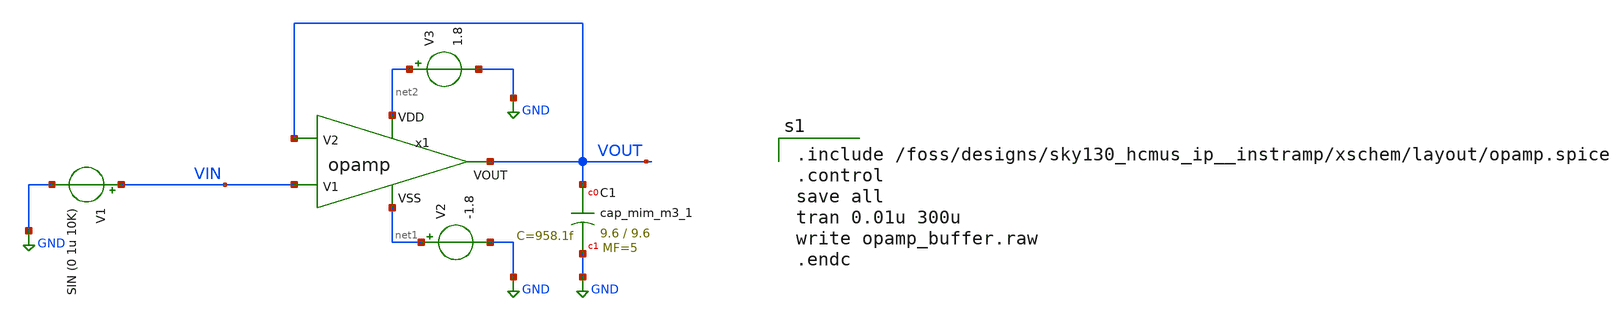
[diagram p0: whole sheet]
** sch_path: xschem/opamp_buffer.sch
**.subckt opamp_buffer
V3 net2 GND 1.8
V2 net1 GND -1.8
V1 VIN GND SIN (0 1u 10K)
x1 net2 net1 VIN VOUT VOUT opamp
XC1 VOUT GND sky130_fd_pr__cap_mim_m3_1 W=9.6 L=9.6 MF=5 m=5
**** begin user architecture code

** opencircuitdesign pdks install
.lib $::SKYWATER_MODELS/sky130.lib.spice tt



.include /foss/designs/sky130_hcmus_ip__instramp/xschem/layout/opamp.spice
.control
save all
tran 0.01u 300u
write opamp_buffer.raw
.endc


**** end user architecture code
**.ends

* expanding   symbol:  /foss/designs/sky130_hcmus_ip__instramp/xschem/opamp.sym # of pins=5
** sym_path: xschem/opamp.sym
** sch_path: xschem/opamp.sch
.subckt opamp VDD VSS V1 V2 VOUT
*.ipin VSS
*.ipin VDD
*.ipin V2
*.ipin V1
*.opin VOUT
XM2 net5 V2 net1 VSS sky130_fd_pr__nfet_01v8 L=1 W=8.5 nf=1 ad='int((nf+1)/2) * W/nf * 0.29' as='int((nf+2)/2) * W/nf * 0.29'
+ pd='2*int((nf+1)/2) * (W/nf + 0.29)' ps='2*int((nf+2)/2) * (W/nf + 0.29)' nrd='0.29 / W' nrs='0.29 / W'
+ sa=0 sb=0 sd=0 mult=1 m=1
XM1 net6 net5 VDD VDD sky130_fd_pr__pfet_01v8 L=1 W=41 nf=1 ad='int((nf+1)/2) * W/nf * 0.29' as='int((nf+2)/2) * W/nf * 0.29'
+ pd='2*int((nf+1)/2) * (W/nf + 0.29)' ps='2*int((nf+2)/2) * (W/nf + 0.29)' nrd='0.29 / W' nrs='0.29 / W'
+ sa=0 sb=0 sd=0 mult=1 m=1
XM4 net6 V1 net1 VSS sky130_fd_pr__nfet_01v8 L=1 W=8.5 nf=1 ad='int((nf+1)/2) * W/nf * 0.29' as='int((nf+2)/2) * W/nf * 0.29'
+ pd='2*int((nf+1)/2) * (W/nf + 0.29)' ps='2*int((nf+2)/2) * (W/nf + 0.29)' nrd='0.29 / W' nrs='0.29 / W'
+ sa=0 sb=0 sd=0 mult=1 m=1
XM5 net1 net4 VSS VSS sky130_fd_pr__nfet_01v8 L=1 W=20 nf=1 ad='int((nf+1)/2) * W/nf * 0.29' as='int((nf+2)/2) * W/nf * 0.29'
+ pd='2*int((nf+1)/2) * (W/nf + 0.29)' ps='2*int((nf+2)/2) * (W/nf + 0.29)' nrd='0.29 / W' nrs='0.29 / W'
+ sa=0 sb=0 sd=0 mult=1 m=1
XM6 VOUT net4 VSS VSS sky130_fd_pr__nfet_01v8 L=1 W=19 nf=1 ad='int((nf+1)/2) * W/nf * 0.29' as='int((nf+2)/2) * W/nf * 0.29'
+ pd='2*int((nf+1)/2) * (W/nf + 0.29)' ps='2*int((nf+2)/2) * (W/nf + 0.29)' nrd='0.29 / W' nrs='0.29 / W'
+ sa=0 sb=0 sd=0 mult=1 m=1
XM7 net4 net4 VSS VSS sky130_fd_pr__nfet_01v8 L=1 W=20 nf=1 ad='int((nf+1)/2) * W/nf * 0.29' as='int((nf+2)/2) * W/nf * 0.29'
+ pd='2*int((nf+1)/2) * (W/nf + 0.29)' ps='2*int((nf+2)/2) * (W/nf + 0.29)' nrd='0.29 / W' nrs='0.29 / W'
+ sa=0 sb=0 sd=0 mult=1 m=1
XM3 net5 net5 VDD VDD sky130_fd_pr__pfet_01v8 L=1 W=41 nf=1 ad='int((nf+1)/2) * W/nf * 0.29' as='int((nf+2)/2) * W/nf * 0.29'
+ pd='2*int((nf+1)/2) * (W/nf + 0.29)' ps='2*int((nf+2)/2) * (W/nf + 0.29)' nrd='0.29 / W' nrs='0.29 / W'
+ sa=0 sb=0 sd=0 mult=1 m=1
XM8 VOUT net6 VDD VDD sky130_fd_pr__pfet_01v8 L=1 W=40 nf=1 ad='int((nf+1)/2) * W/nf * 0.29' as='int((nf+2)/2) * W/nf * 0.29'
+ pd='2*int((nf+1)/2) * (W/nf + 0.29)' ps='2*int((nf+2)/2) * (W/nf + 0.29)' nrd='0.29 / W' nrs='0.29 / W'
+ sa=0 sb=0 sd=0 mult=2 m=2
XR3 net2 VDD VSS sky130_fd_pr__res_high_po W=1 L=50 mult=1 m=1
XR1 net3 net2 VSS sky130_fd_pr__res_high_po W=1 L=50 mult=1 m=1
XR2 net4 net3 VSS sky130_fd_pr__res_high_po W=1 L=50 mult=1 m=1
XR4 net7 VOUT VSS sky130_fd_pr__res_high_po W=1 L=7 mult=1 m=1
XC1 net7 net6 sky130_fd_pr__cap_mim_m3_1 W=5.55 L=10 MF=20 m=20
.ends

.GLOBAL GND
.end
